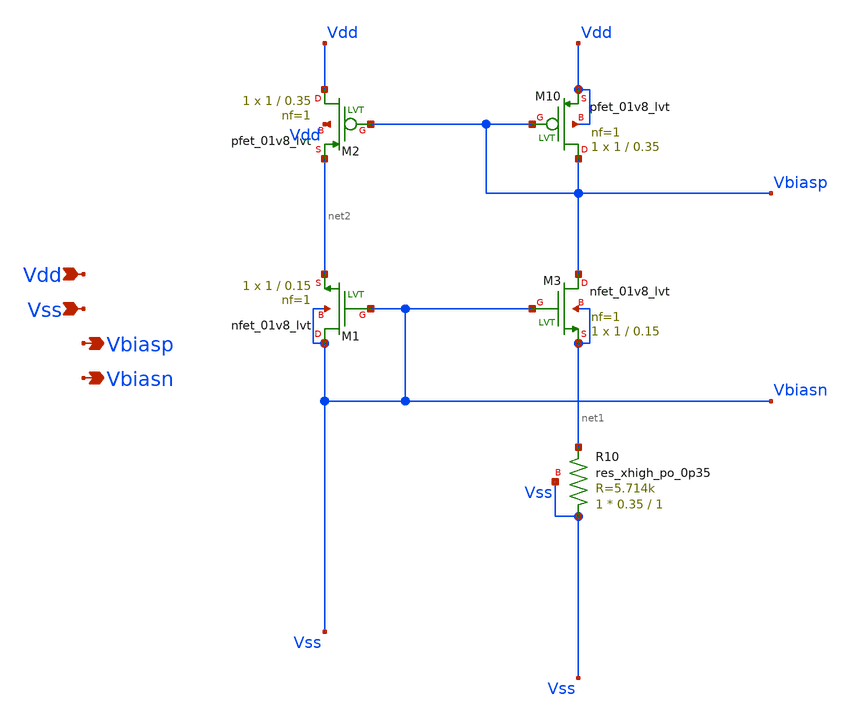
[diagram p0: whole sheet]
** sch_path: tt10-hdl/tt_um_test_commit/xschem/T2/biasGen/Z_old/basic_currSrc.sch
**.subckt basic_currSrc Vdd Vss Vbiasp Vbiasn
*.ipin Vdd
*.ipin Vss
*.opin Vbiasp
*.opin Vbiasn
XM10 Vbiasp Vbiasp Vdd Vdd sky130_fd_pr__pfet_01v8_lvt L=0.35 W=1 nf=1 ad='int((1 + 1)/2) * 1 / 1 * 0.29'
+ as='int((1 + 2)/2) * 1 / 1 * 0.29' pd='2*int((1 + 1)/2) * (1 / 1 + 0.29)' ps='2*int((1 + 2)/2) * (1 / 1 + 0.29)'
+ nrd='0.29 / 1 ' nrs='0.29 / 1 ' sa=0 sb=0 sd=0 mult=1 m=1
XM1 Vss Vss net2 Vss sky130_fd_pr__nfet_01v8_lvt L=0.15 W=1 nf=1 ad='int((1 + 1)/2) * 1 / 1 * 0.29' as='int((1 + 2)/2) * 1 / 1 * 0.29'
+ pd='2*int((1 + 1)/2) * (1 / 1 + 0.29)' ps='2*int((1 + 2)/2) * (1 / 1 + 0.29)' nrd='0.29 / 1 ' nrs='0.29 / 1 '
+ sa=0 sb=0 sd=0 mult=1 m=1
XR10 Vss net1 Vss sky130_fd_pr__res_xhigh_po_0p35 L=1 mult=1 m=1
XM2 Vdd Vbiasp net2 Vdd sky130_fd_pr__pfet_01v8_lvt L=0.35 W=1 nf=1 ad='int((1 + 1)/2) * 1 / 1 * 0.29'
+ as='int((1 + 2)/2) * 1 / 1 * 0.29' pd='2*int((1 + 1)/2) * (1 / 1 + 0.29)' ps='2*int((1 + 2)/2) * (1 / 1 + 0.29)'
+ nrd='0.29 / 1 ' nrs='0.29 / 1 ' sa=0 sb=0 sd=0 mult=1 m=1
XM3 Vbiasp Vss net1 net1 sky130_fd_pr__nfet_01v8_lvt L=0.15 W=1 nf=1 ad='int((1 + 1)/2) * 1 / 1 * 0.29'
+ as='int((1 + 2)/2) * 1 / 1 * 0.29' pd='2*int((1 + 1)/2) * (1 / 1 + 0.29)' ps='2*int((1 + 2)/2) * (1 / 1 + 0.29)'
+ nrd='0.29 / 1 ' nrs='0.29 / 1 ' sa=0 sb=0 sd=0 mult=1 m=1
**.ends
.end
